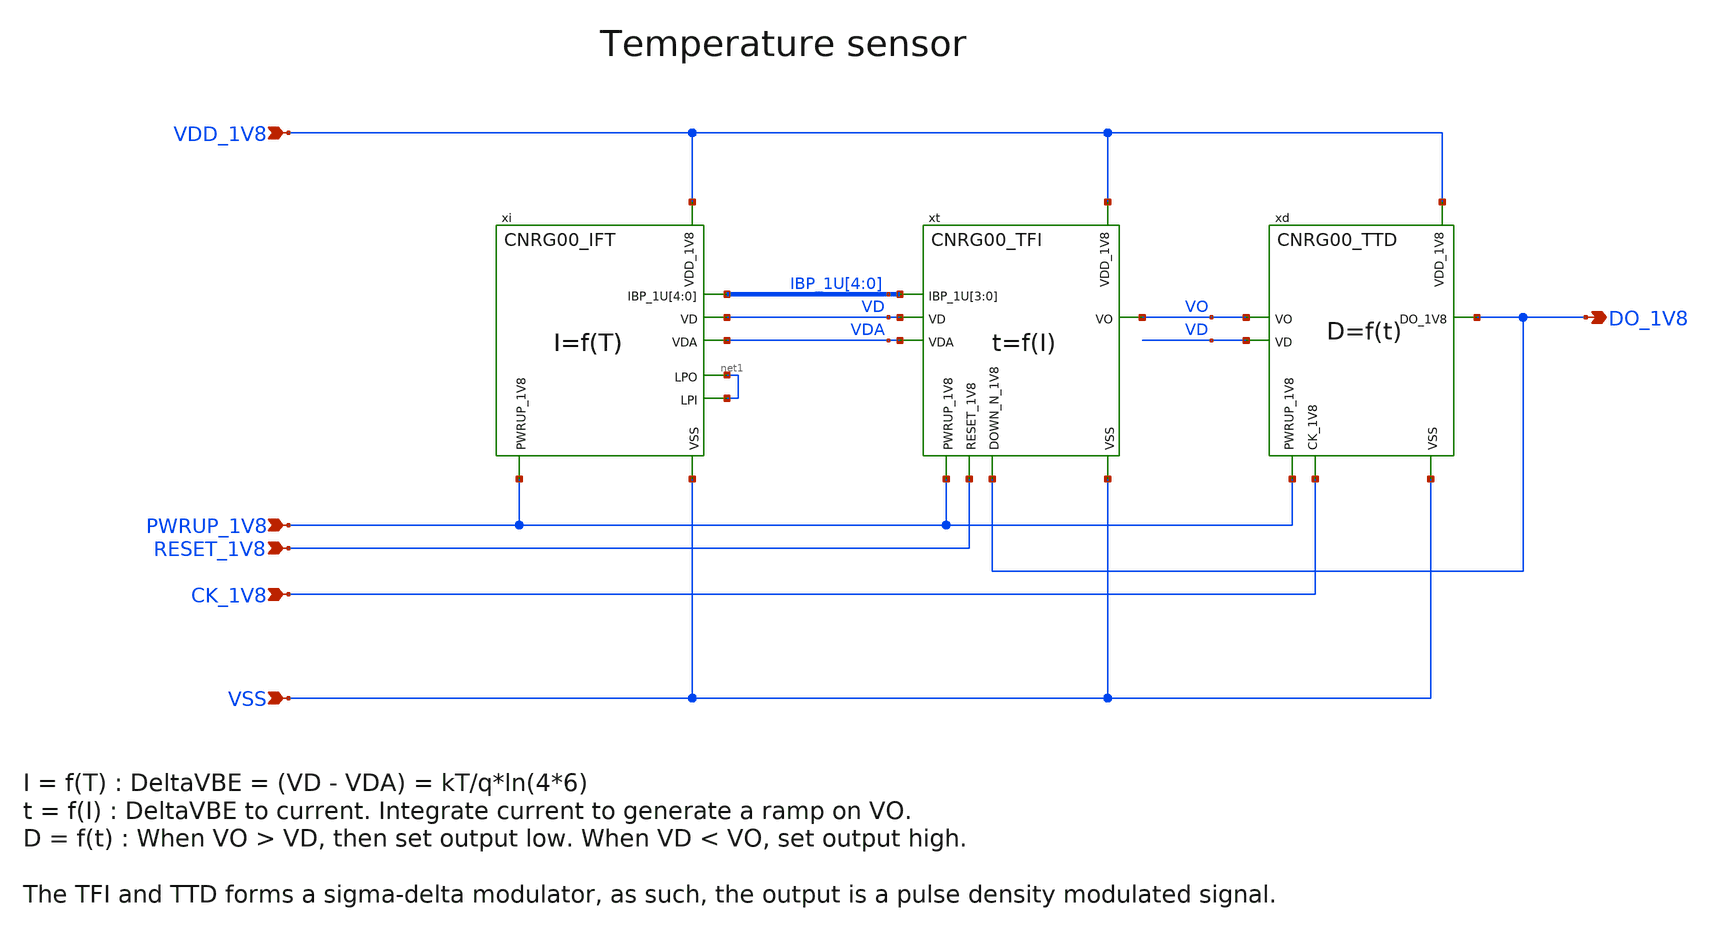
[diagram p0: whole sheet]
** sch_path: design/CNR_GR00_SKY130NM/CNR_GR00.sch
**.subckt CNR_GR00 VDD_1V8 VSS PWRUP_1V8 RESET_1V8 DO_1V8 CK_1V8
*.ipin VDD_1V8
*.ipin VSS
*.ipin PWRUP_1V8
*.ipin RESET_1V8
*.opin DO_1V8
*.ipin CK_1V8
xi VDD_1V8 IBP_1U[4] IBP_1U[3] IBP_1U[2] IBP_1U[1] IBP_1U[0] VD VDA PWRUP_1V8 VSS net1 net1
+ CNRG00_IFT
xt RESET_1V8 VDD_1V8 VD VO PWRUP_1V8 VDA IBP_1U[4] IBP_1U[3] IBP_1U[2] IBP_1U[1] VSS DO_1V8
+ CNRG00_TFI
xd VDD_1V8 VD DO_1V8 VO CK_1V8 VSS PWRUP_1V8 CNRG00_TTD
**.ends
.end
